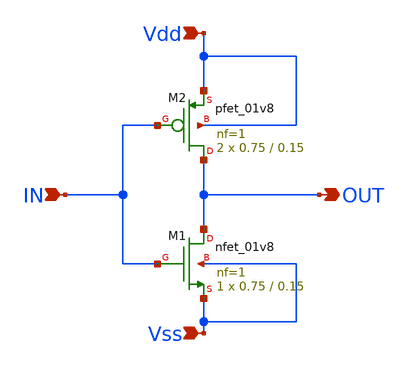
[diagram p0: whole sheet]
** sch_path: icdesign/sch/Inversor/Inversor.sch
**.subckt Inversor IN Vdd Vss OUT
*.ipin IN
*.ipin Vdd
*.ipin Vss
*.opin OUT
XM1 OUT IN Vss Vss sky130_fd_pr__nfet_01v8 L=0.15 W=0.75 nf=1 ad='int((nf+1)/2) * W/nf * 0.29' as='int((nf+2)/2) * W/nf * 0.29'
+ pd='2*int((nf+1)/2) * (W/nf + 0.29)' ps='2*int((nf+2)/2) * (W/nf + 0.29)' nrd='0.29 / W' nrs='0.29 / W'
+ sa=0 sb=0 sd=0 mult=1 m=1
XM2 OUT IN Vdd Vdd sky130_fd_pr__pfet_01v8 L=0.15 W=0.75 nf=1 ad='int((nf+1)/2) * W/nf * 0.29' as='int((nf+2)/2) * W/nf * 0.29'
+ pd='2*int((nf+1)/2) * (W/nf + 0.29)' ps='2*int((nf+2)/2) * (W/nf + 0.29)' nrd='0.29 / W' nrs='0.29 / W'
+ sa=0 sb=0 sd=0 mult=2 m=2
**.ends
.end
